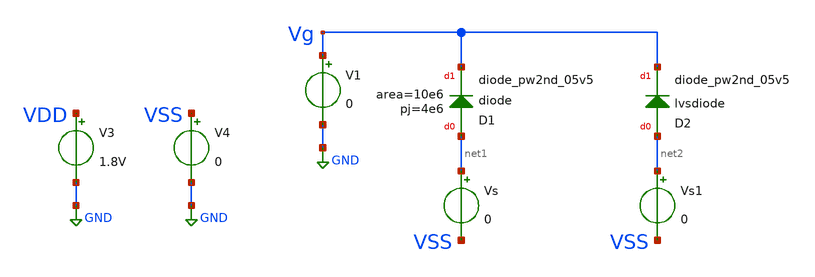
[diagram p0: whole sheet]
** sch_path: xschem/tests/dummy_tests/dummy_diod.sch
**.subckt dummy_diod
V3 VDD GND 1.8V
V4 VSS GND 0
V1 Vg GND 0
Vs net1 VSS 0
XD1 net1 Vg sky130_fd_pr__diode_pw2nd_05v5 area=10e6 pj=4e6
D2 net2 Vg sky130_fd_pr__diode_pw2nd_05v5 area=10e6
Vs1 net2 VSS 0
**** begin user architecture code
 .lib $::SKYWATER_MODELS/sky130.lib.spice tt
.include $::SKYWATER_STDCELLS/sky130_fd_sc_hd.spice


.options acct list
.temp 25
*vvcc VDD 0 dc 1.8
*vvss VSS 0 0
.control
*tran 0.1u 400u
dc v1 0 10V 0.1
*plot RST_PLS clk+2 Pulse+4
plot Vg-Vss
plot i(Vs) i(Vs1)
write pulse_generator_test.raw
.endc


**** end user architecture code
**.ends
.GLOBAL GND
.end
